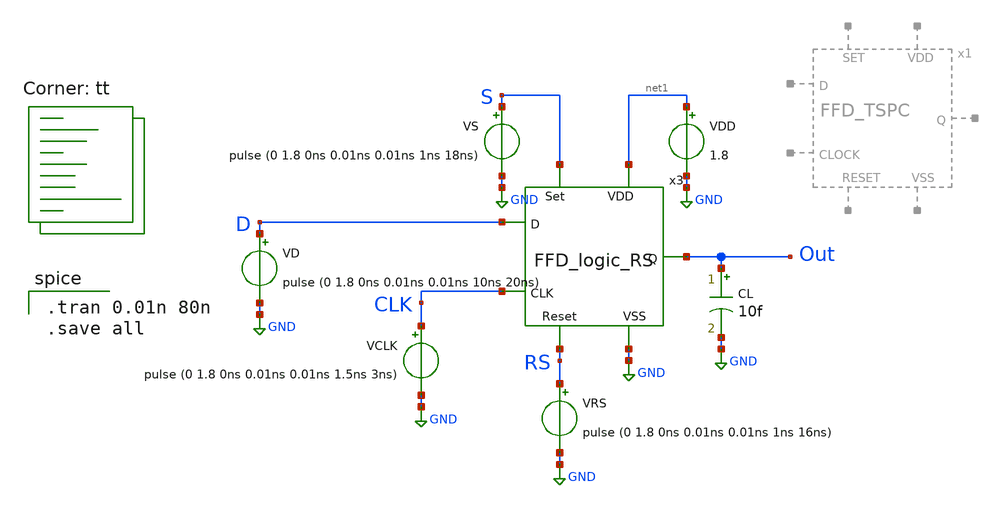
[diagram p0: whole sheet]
** sch_path: FFD_TSPC_tb.sch
**.subckt FFD_TSPC_tb
CL Out GND 10f m=1
VD D GND pulse (0 1.8 0ns 0.01ns 0.01ns 10ns 20ns)
VCLK CLK GND pulse (0 1.8 0ns 0.01ns 0.01ns 1.5ns 3ns)
VRS RS GND pulse (0 1.8 0ns 0.01ns 0.01ns 1ns 16ns)
VS S GND pulse (0 1.8 0ns 0.01ns 0.01ns 1ns 18ns)
VDD net1 GND 1.8
x3 S net1 Out CLK D GND RS FFD_logic_RS
**** begin user architecture code
.lib $::SKYWATER_MODELS/sky130.lib.spice tt

.tran 0.01n 80n
.save all

**** end user architecture code
**.ends

* expanding   symbol:  project/FFD_TSPC.sym # of pins=7
** sym_path: FFD_TSPC.sym
** sch_path: FFD_TSPC.sch
.subckt FFD_TSPC VDD VSS SET CLOCK RESET D Q
*.ipin CLOCK
*.ipin SET
*.ipin RESET
*.ipin VDD
*.ipin VSS
*.ipin D
*.opin Q
XM1 net2 D VSS VSS sky130_fd_pr__nfet_01v8 L=0.15 W=0.5 nf=1 ad='int((nf+1)/2) * W/nf * 0.29' as='int((nf+2)/2) * W/nf * 0.29'
+ pd='2*int((nf+1)/2) * (W/nf + 0.29)' ps='2*int((nf+2)/2) * (W/nf + 0.29)' nrd='0.29 / W' nrs='0.29 / W'
+ sa=0 sb=0 sd=0 mult=1 m=1
XM2 net3 CLOCK VSS VSS sky130_fd_pr__nfet_01v8 L=0.15 W=0.5 nf=1 ad='int((nf+1)/2) * W/nf * 0.29' as='int((nf+2)/2) * W/nf * 0.29'
+ pd='2*int((nf+1)/2) * (W/nf + 0.29)' ps='2*int((nf+2)/2) * (W/nf + 0.29)' nrd='0.29 / W' nrs='0.29 / W'
+ sa=0 sb=0 sd=0 mult=1 m=1
XM3 net4 Q_pre VSS VSS sky130_fd_pr__nfet_01v8 L=0.15 W=0.5 nf=1 ad='int((nf+1)/2) * W/nf * 0.29' as='int((nf+2)/2) * W/nf * 0.29'
+ pd='2*int((nf+1)/2) * (W/nf + 0.29)' ps='2*int((nf+2)/2) * (W/nf + 0.29)' nrd='0.29 / W' nrs='0.29 / W'
+ sa=0 sb=0 sd=0 mult=1 m=1
XM4 net2 CLOCK net1 VDD sky130_fd_pr__pfet_01v8 L=0.15 W=2 nf=1 ad='int((nf+1)/2) * W/nf * 0.29' as='int((nf+2)/2) * W/nf * 0.29'
+ pd='2*int((nf+1)/2) * (W/nf + 0.29)' ps='2*int((nf+2)/2) * (W/nf + 0.29)' nrd='0.29 / W' nrs='0.29 / W'
+ sa=0 sb=0 sd=0 mult=1 m=1
XM5 Q_pre net2 net3 VSS sky130_fd_pr__nfet_01v8 L=0.15 W=0.5 nf=1 ad='int((nf+1)/2) * W/nf * 0.29' as='int((nf+2)/2) * W/nf * 0.29'
+ pd='2*int((nf+1)/2) * (W/nf + 0.29)' ps='2*int((nf+2)/2) * (W/nf + 0.29)' nrd='0.29 / W' nrs='0.29 / W'
+ sa=0 sb=0 sd=0 mult=1 m=1
XM6 QB_pre CLOCK net4 VSS sky130_fd_pr__nfet_01v8 L=0.15 W=0.5 nf=1 ad='int((nf+1)/2) * W/nf * 0.29'
+ as='int((nf+2)/2) * W/nf * 0.29' pd='2*int((nf+1)/2) * (W/nf + 0.29)' ps='2*int((nf+2)/2) * (W/nf + 0.29)'
+ nrd='0.29 / W' nrs='0.29 / W' sa=0 sb=0 sd=0 mult=1 m=1
XM7 Q QB_pre VSS VSS sky130_fd_pr__nfet_01v8 L=0.15 W=3 nf=1 ad='int((nf+1)/2) * W/nf * 0.29' as='int((nf+2)/2) * W/nf * 0.29'
+ pd='2*int((nf+1)/2) * (W/nf + 0.29)' ps='2*int((nf+2)/2) * (W/nf + 0.29)' nrd='0.29 / W' nrs='0.29 / W'
+ sa=0 sb=0 sd=0 mult=1 m=1
XM8 net1 D VDD VDD sky130_fd_pr__pfet_01v8 L=0.15 W=2 nf=1 ad='int((nf+1)/2) * W/nf * 0.29' as='int((nf+2)/2) * W/nf * 0.29'
+ pd='2*int((nf+1)/2) * (W/nf + 0.29)' ps='2*int((nf+2)/2) * (W/nf + 0.29)' nrd='0.29 / W' nrs='0.29 / W'
+ sa=0 sb=0 sd=0 mult=1 m=1
XM9 Q_pre CLOCK VDD VDD sky130_fd_pr__pfet_01v8 L=0.15 W=2 nf=1 ad='int((nf+1)/2) * W/nf * 0.29' as='int((nf+2)/2) * W/nf * 0.29'
+ pd='2*int((nf+1)/2) * (W/nf + 0.29)' ps='2*int((nf+2)/2) * (W/nf + 0.29)' nrd='0.29 / W' nrs='0.29 / W'
+ sa=0 sb=0 sd=0 mult=1 m=1
XM10 net5 Q_pre VDD VDD sky130_fd_pr__pfet_01v8 L=0.15 W=2 nf=1 ad='int((nf+1)/2) * W/nf * 0.29' as='int((nf+2)/2) * W/nf * 0.29'
+ pd='2*int((nf+1)/2) * (W/nf + 0.29)' ps='2*int((nf+2)/2) * (W/nf + 0.29)' nrd='0.29 / W' nrs='0.29 / W'
+ sa=0 sb=0 sd=0 mult=1 m=1
XM11 QB_pre RS VDD VDD sky130_fd_pr__pfet_01v8 L=0.15 W=2 nf=1 ad='int((nf+1)/2) * W/nf * 0.29' as='int((nf+2)/2) * W/nf * 0.29'
+ pd='2*int((nf+1)/2) * (W/nf + 0.29)' ps='2*int((nf+2)/2) * (W/nf + 0.29)' nrd='0.29 / W' nrs='0.29 / W'
+ sa=0 sb=0 sd=0 mult=1 m=1
XM12 Q QB_pre VDD VDD sky130_fd_pr__pfet_01v8 L=0.15 W=6 nf=1 ad='int((nf+1)/2) * W/nf * 0.29' as='int((nf+2)/2) * W/nf * 0.29'
+ pd='2*int((nf+1)/2) * (W/nf + 0.29)' ps='2*int((nf+2)/2) * (W/nf + 0.29)' nrd='0.29 / W' nrs='0.29 / W'
+ sa=0 sb=0 sd=0 mult=1 m=1
XM13 QB_pre SET VSS VSS sky130_fd_pr__nfet_01v8 L=0.15 W=0.5 nf=1 ad='int((nf+1)/2) * W/nf * 0.29' as='int((nf+2)/2) * W/nf * 0.29'
+ pd='2*int((nf+1)/2) * (W/nf + 0.29)' ps='2*int((nf+2)/2) * (W/nf + 0.29)' nrd='0.29 / W' nrs='0.29 / W'
+ sa=0 sb=0 sd=0 mult=1 m=1
x1 VDD RESET RS VSS Inverter
XM14 QB_pre SET net5 VDD sky130_fd_pr__pfet_01v8 L=0.15 W=2 nf=1 ad='int((nf+1)/2) * W/nf * 0.29' as='int((nf+2)/2) * W/nf * 0.29'
+ pd='2*int((nf+1)/2) * (W/nf + 0.29)' ps='2*int((nf+2)/2) * (W/nf + 0.29)' nrd='0.29 / W' nrs='0.29 / W'
+ sa=0 sb=0 sd=0 mult=1 m=1
.ends


* expanding   symbol:  Thesis/FFD_logic_RS.sym # of pins=7
** sym_path: FFD_logic_RS.sym
** sch_path: FFD_logic_RS.sch
.subckt FFD_logic_RS Set VDD Q CLK D VSS Reset
*.ipin D
*.ipin CLK
*.ipin VDD
*.ipin VSS
*.opin Q
*.ipin Set
*.ipin Reset
x1 VDD net3 D net2 VSS nand_FFD
x2 VDD net4 net2 net1 VSS nand_FFD
x5 VDD net8 net5 CLK VSS nand_FFD
x6 VDD net7 CLK net6 VSS nand_FFD
x9 VDD D net1 VSS Inverter
x10 VDD CLK net2 VSS Inverter
x3 net6 VDD net5 net10 net3 VSS nand_FFD_3pin
x4 net11 VDD net6 net5 net4 VSS nand_FFD_3pin
x7 net9 VDD Q net10 net8 VSS nand_FFD_3pin
x8 net11 VDD net9 Q net7 VSS nand_FFD_3pin
x11 VDD Set net10 VSS Inverter
x12 VDD Reset net11 VSS Inverter
.ends


* expanding   symbol:  Inverter.sym # of pins=4
** sym_path: Inverter.sym
** sch_path: Inverter.sch
.subckt Inverter VDD IN OUT VSS
*.ipin IN
*.ipin VSS
*.ipin VDD
*.opin OUT
XM1 OUT IN VSS VSS sky130_fd_pr__nfet_01v8 L=0.3 W=1 nf=1 ad='int((nf+1)/2) * W/nf * 0.29' as='int((nf+2)/2) * W/nf * 0.29'
+ pd='2*int((nf+1)/2) * (W/nf + 0.29)' ps='2*int((nf+2)/2) * (W/nf + 0.29)' nrd='0.29 / W' nrs='0.29 / W'
+ sa=0 sb=0 sd=0 mult=1 m=1
XM2 OUT IN VDD VDD sky130_fd_pr__pfet_01v8 L=0.3 W=2 nf=1 ad='int((nf+1)/2) * W/nf * 0.29' as='int((nf+2)/2) * W/nf * 0.29'
+ pd='2*int((nf+1)/2) * (W/nf + 0.29)' ps='2*int((nf+2)/2) * (W/nf + 0.29)' nrd='0.29 / W' nrs='0.29 / W'
+ sa=0 sb=0 sd=0 mult=1 m=1
.ends


* expanding   symbol:  nand_FFD.sym # of pins=5
** sym_path: nand_FFD.sym
** sch_path: nand_FFD.sch
.subckt nand_FFD VDD Y A B VSS
*.ipin VDD
*.ipin A
*.ipin B
*.ipin VSS
*.opin Y
XM1 Y A net1 VSS sky130_fd_pr__nfet_01v8 L=0.15 W=1 nf=1 ad='int((nf+1)/2) * W/nf * 0.29' as='int((nf+2)/2) * W/nf * 0.29'
+ pd='2*int((nf+1)/2) * (W/nf + 0.29)' ps='2*int((nf+2)/2) * (W/nf + 0.29)' nrd='0.29 / W' nrs='0.29 / W'
+ sa=0 sb=0 sd=0 mult=1 m=1
XM2 net1 B VSS VSS sky130_fd_pr__nfet_01v8 L=0.15 W=1 nf=1 ad='int((nf+1)/2) * W/nf * 0.29' as='int((nf+2)/2) * W/nf * 0.29'
+ pd='2*int((nf+1)/2) * (W/nf + 0.29)' ps='2*int((nf+2)/2) * (W/nf + 0.29)' nrd='0.29 / W' nrs='0.29 / W'
+ sa=0 sb=0 sd=0 mult=1 m=1
XM3 Y A VDD VDD sky130_fd_pr__pfet_01v8 L=0.15 W=2 nf=1 ad='int((nf+1)/2) * W/nf * 0.29' as='int((nf+2)/2) * W/nf * 0.29'
+ pd='2*int((nf+1)/2) * (W/nf + 0.29)' ps='2*int((nf+2)/2) * (W/nf + 0.29)' nrd='0.29 / W' nrs='0.29 / W'
+ sa=0 sb=0 sd=0 mult=1 m=1
XM4 Y B VDD VDD sky130_fd_pr__pfet_01v8 L=0.15 W=2 nf=1 ad='int((nf+1)/2) * W/nf * 0.29' as='int((nf+2)/2) * W/nf * 0.29'
+ pd='2*int((nf+1)/2) * (W/nf + 0.29)' ps='2*int((nf+2)/2) * (W/nf + 0.29)' nrd='0.29 / W' nrs='0.29 / W'
+ sa=0 sb=0 sd=0 mult=1 m=1
.ends


* expanding   symbol:  Thesis/nand_FFD_3pin.sym # of pins=6
** sym_path: nand_FFD_3pin.sym
** sch_path: nand_FFD_3pin.sch
.subckt nand_FFD_3pin C VDD Y A B VSS
*.ipin VDD
*.ipin A
*.ipin B
*.ipin VSS
*.opin Y
*.ipin C
XM1 Y A net1 VSS sky130_fd_pr__nfet_01v8 L=0.15 W=1 nf=1 ad='int((nf+1)/2) * W/nf * 0.29' as='int((nf+2)/2) * W/nf * 0.29'
+ pd='2*int((nf+1)/2) * (W/nf + 0.29)' ps='2*int((nf+2)/2) * (W/nf + 0.29)' nrd='0.29 / W' nrs='0.29 / W'
+ sa=0 sb=0 sd=0 mult=1 m=1
XM2 net1 B net2 VSS sky130_fd_pr__nfet_01v8 L=0.15 W=1 nf=1 ad='int((nf+1)/2) * W/nf * 0.29' as='int((nf+2)/2) * W/nf * 0.29'
+ pd='2*int((nf+1)/2) * (W/nf + 0.29)' ps='2*int((nf+2)/2) * (W/nf + 0.29)' nrd='0.29 / W' nrs='0.29 / W'
+ sa=0 sb=0 sd=0 mult=1 m=1
XM3 Y A VDD VDD sky130_fd_pr__pfet_01v8 L=0.15 W=2 nf=1 ad='int((nf+1)/2) * W/nf * 0.29' as='int((nf+2)/2) * W/nf * 0.29'
+ pd='2*int((nf+1)/2) * (W/nf + 0.29)' ps='2*int((nf+2)/2) * (W/nf + 0.29)' nrd='0.29 / W' nrs='0.29 / W'
+ sa=0 sb=0 sd=0 mult=1 m=1
XM4 Y B VDD VDD sky130_fd_pr__pfet_01v8 L=0.15 W=2 nf=1 ad='int((nf+1)/2) * W/nf * 0.29' as='int((nf+2)/2) * W/nf * 0.29'
+ pd='2*int((nf+1)/2) * (W/nf + 0.29)' ps='2*int((nf+2)/2) * (W/nf + 0.29)' nrd='0.29 / W' nrs='0.29 / W'
+ sa=0 sb=0 sd=0 mult=1 m=1
XM5 Y C VDD VDD sky130_fd_pr__pfet_01v8 L=0.15 W=2 nf=1 ad='int((nf+1)/2) * W/nf * 0.29' as='int((nf+2)/2) * W/nf * 0.29'
+ pd='2*int((nf+1)/2) * (W/nf + 0.29)' ps='2*int((nf+2)/2) * (W/nf + 0.29)' nrd='0.29 / W' nrs='0.29 / W'
+ sa=0 sb=0 sd=0 mult=1 m=1
XM6 net2 C VSS VSS sky130_fd_pr__nfet_01v8 L=0.15 W=1 nf=1 ad='int((nf+1)/2) * W/nf * 0.29' as='int((nf+2)/2) * W/nf * 0.29'
+ pd='2*int((nf+1)/2) * (W/nf + 0.29)' ps='2*int((nf+2)/2) * (W/nf + 0.29)' nrd='0.29 / W' nrs='0.29 / W'
+ sa=0 sb=0 sd=0 mult=1 m=1
.ends

.GLOBAL GND
.end
